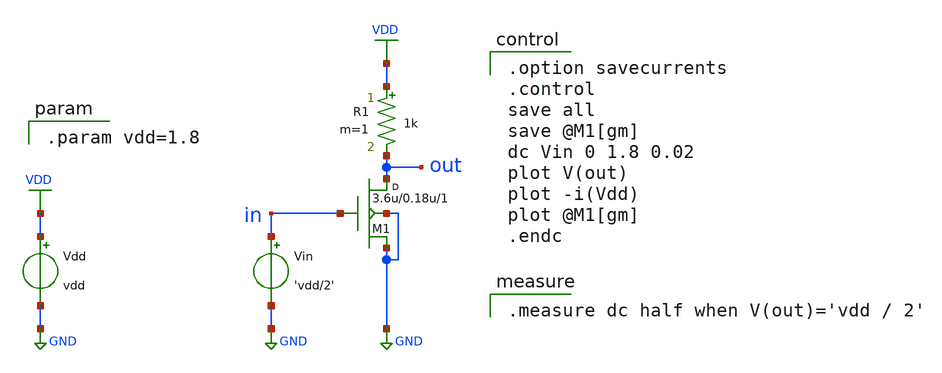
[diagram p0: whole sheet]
** sch_path: xschem/tb/dc_02_param.sch
**.subckt dc_02_param
Vdd VDD GND vdd
Vin in GND 'vdd/2'
R1 VDD out 1k m=1
M1 out in GND GND nch w=3.6u l=0.18u m=1
**** begin user architecture code

.model nch nmos ( version=4.7 level=54 lmin=0.1u lmax=20u wmin=0.1u wmax=10u  )
.model pch pmos ( version=4.7 level=54 lmin=0.1u lmax=20u wmin=0.1u wmax=10u  )


.option savecurrents
.control
save all
save @M1[gm]
dc Vin 0 1.8 0.02
plot V(out)
plot -i(Vdd)
plot @M1[gm]
.endc


.measure dc half when V(out)='vdd / 2'


.param vdd=1.8

**** end user architecture code
**.ends
.GLOBAL VDD
.GLOBAL GND
.end
